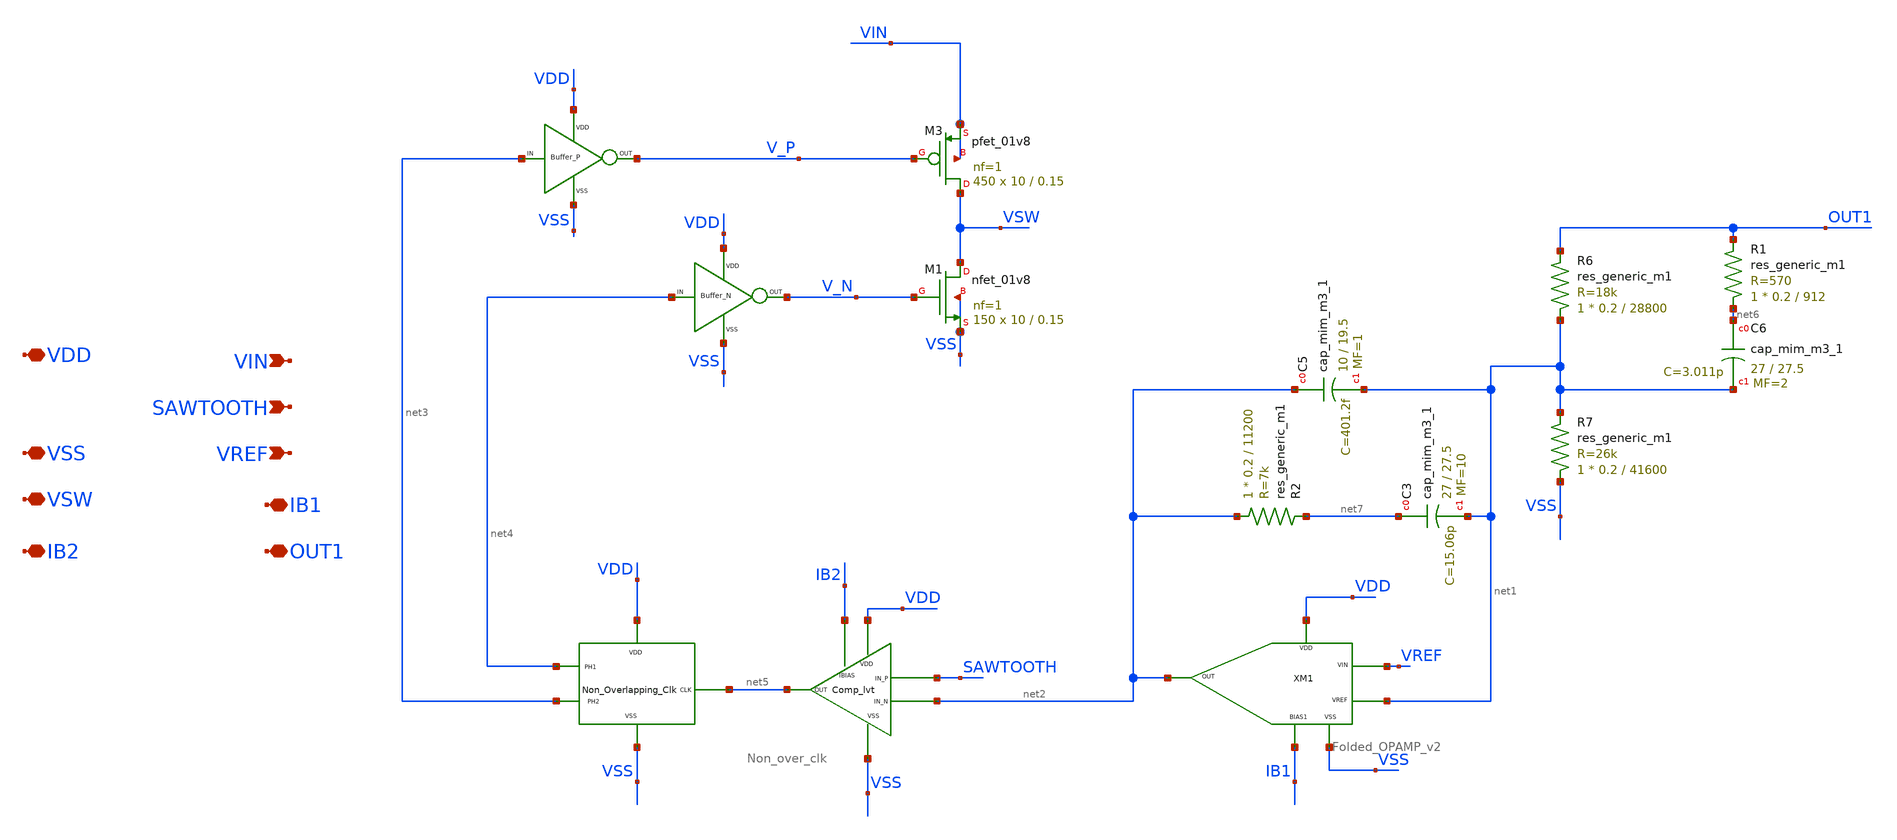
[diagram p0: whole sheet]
** sch_path: xschem/DC_DC_Converter_xschem/OTHERS/DC_DC_Converter_JV10/TOP_LEVEL/Top_Final/Top_1.sch
**.subckt Top_1 VIN VDD VSS IB2 SAWTOOTH VREF IB1 VSW OUT1
*.ipin VIN
*.iopin VDD
*.iopin VSS
*.iopin IB2
*.ipin SAWTOOTH
*.ipin VREF
*.iopin IB1
*.iopin VSW
*.iopin OUT1
XM3 VSW V_P VIN VIN sky130_fd_pr__pfet_01v8 L=0.15 W=10 nf=1 ad='int((nf+1)/2) * W/nf * 0.29' as='int((nf+2)/2) * W/nf * 0.29'
+ pd='2*int((nf+1)/2) * (W/nf + 0.29)' ps='2*int((nf+2)/2) * (W/nf + 0.29)' nrd='0.29 / W' nrs='0.29 / W'
+ sa=0 sb=0 sd=0 mult=450 m=450
XM1 VSW V_N VSS VSS sky130_fd_pr__nfet_01v8 L=0.15 W=10 nf=1 ad='int((nf+1)/2) * W/nf * 0.29' as='int((nf+2)/2) * W/nf * 0.29'
+ pd='2*int((nf+1)/2) * (W/nf + 0.29)' ps='2*int((nf+2)/2) * (W/nf + 0.29)' nrd='0.29 / W' nrs='0.29 / W'
+ sa=0 sb=0 sd=0 mult=150 m=150
X1 net3 V_P VDD VSS BUFFER_P
X2 net4 V_N VDD VSS BUFFER_N
XM3 net5 VDD VSS net4 net3 Non_over_clk
XM2 IB2 VDD SAWTOOTH net2 VSS net5 Comp_lvt
R1 net6 OUT1 sky130_fd_pr__res_generic_m1 W=0.2 L=912 m=1
R6 net1 OUT1 sky130_fd_pr__res_generic_m1 W=0.2 L=28800 m=1
R7 VSS net1 sky130_fd_pr__res_generic_m1 W=0.2 L=41600 m=1
XC6 net6 net1 sky130_fd_pr__cap_mim_m3_1 W=27 L=27.5 MF=2 m=2
XC5 net2 net1 sky130_fd_pr__cap_mim_m3_1 W=10 L=19.5 MF=1 m=1
XC3 net7 net1 sky130_fd_pr__cap_mim_m3_1 W=27 L=27.5 MF=10 m=10
R2 net2 net7 sky130_fd_pr__res_generic_m1 W=0.2 L=11200 m=1
XM1 VDD VSS IB1 net2 VREF net1 Folded_OPAMP_v2
**.ends
.end
